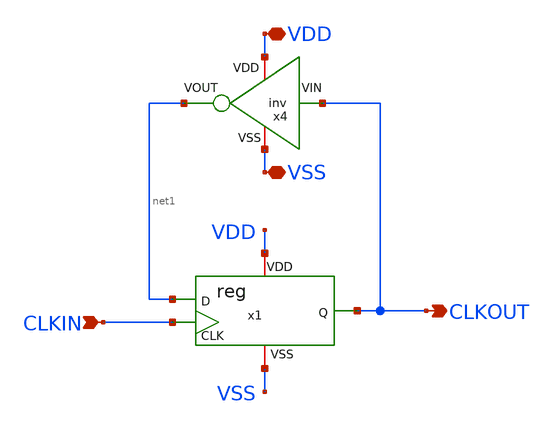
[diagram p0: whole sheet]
** sch_path: Custom_std_cells/reg_inv.sch
**.subckt reg_inv VDD VSS CLKIN CLKOUT
*.iopin VDD
*.iopin VSS
*.ipin CLKIN
*.opin CLKOUT
x1 VDD CLKIN CLKOUT net1 VSS reg
x4 VDD net1 CLKOUT VSS inv
**.ends
.end
